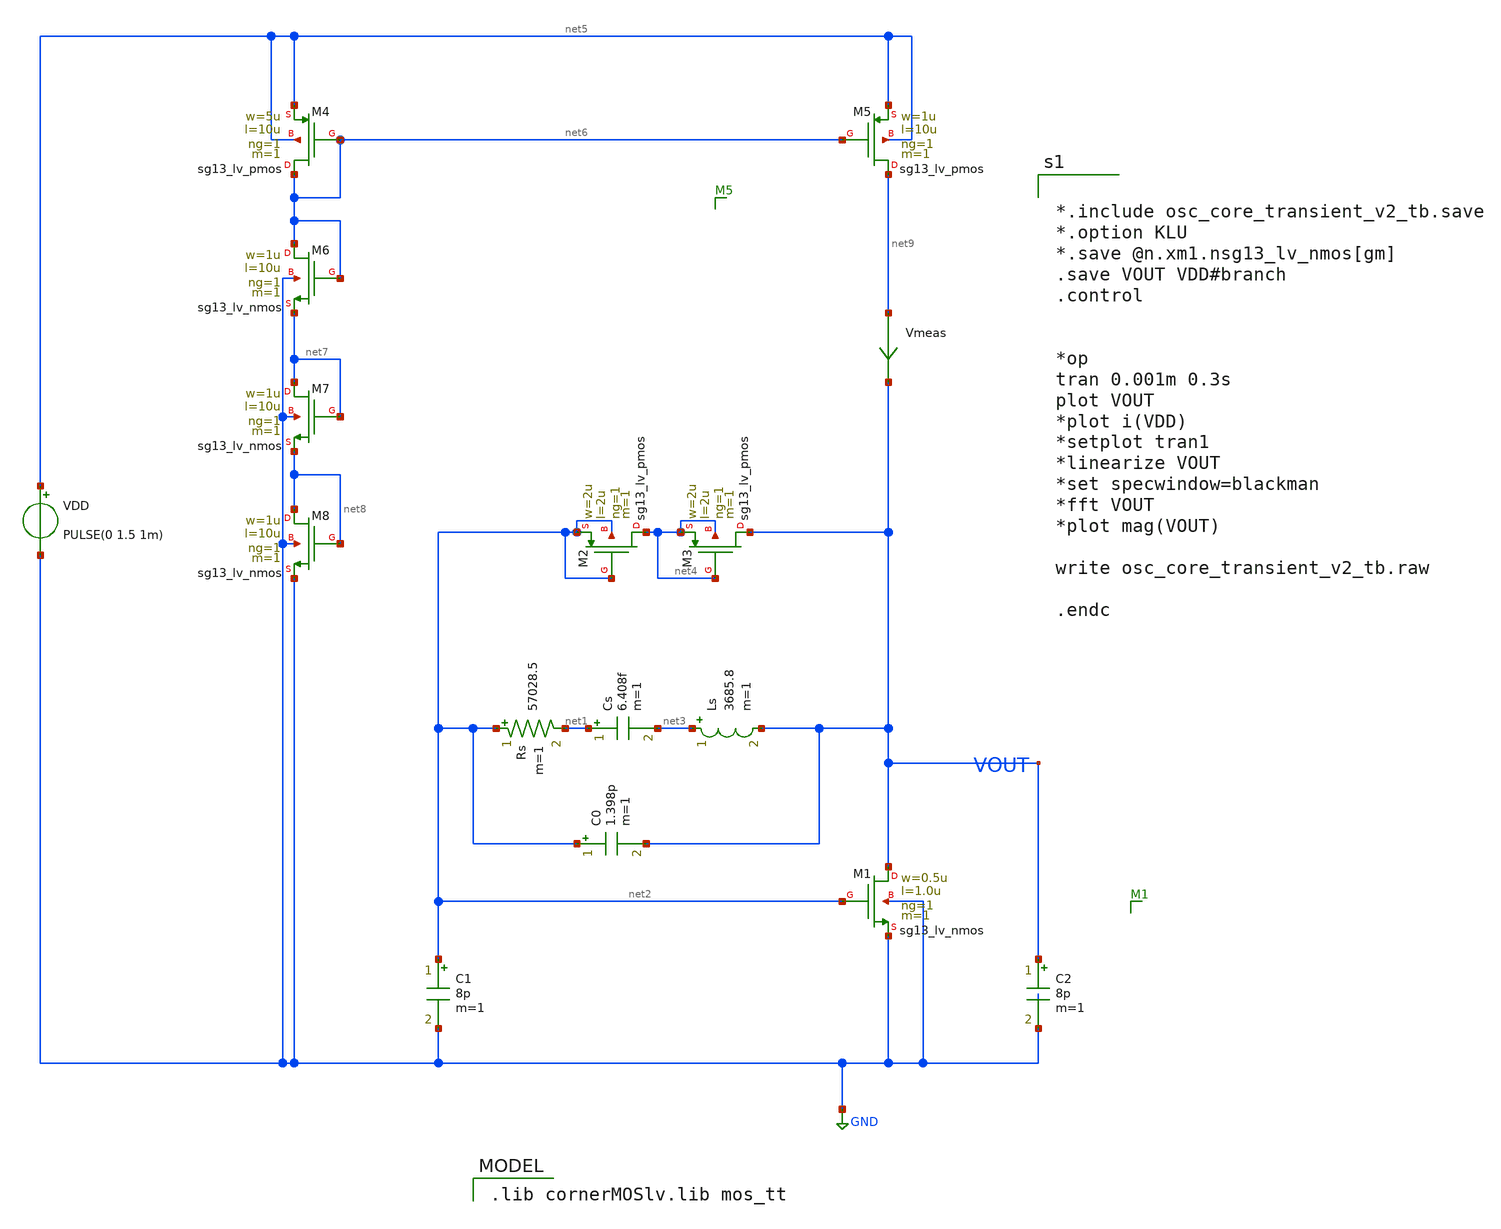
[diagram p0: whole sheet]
** sch_path: osc_core_transient_v2_tb.sch
**.subckt osc_core_transient_v2_tb
XM1 VOUT net2 GND GND sg13_lv_nmos w=0.5u l=1.0u ng=1 m=1 mm_ok=1
C1 net2 GND 8p m=1
C2 VOUT GND 8p m=1
Rs net2 net1 57028.5 m=1
Cs net1 net3 6.408f m=1
C0 net2 VOUT 1.398p m=1
Ls net3 VOUT 3685.8 m=1
VDD net5 GND PULSE(0 1.5 1m)
XM2 net4 net2 net2 net2 sg13_lv_pmos w=2u l=2u ng=1 m=1 mm_ok=1
XM3 VOUT net4 net4 net4 sg13_lv_pmos w=2u l=2u ng=1 m=1 mm_ok=1
XM4 net6 net6 net5 net5 sg13_lv_pmos w=5u l=10u ng=1 m=1 mm_ok=1
XM5 net9 net6 net5 net5 sg13_lv_pmos w=1u l=10u ng=1 m=1 mm_ok=1
XM6 net6 net6 net7 GND sg13_lv_nmos w=1u l=10u ng=1 m=1 mm_ok=1
XM7 net7 net7 net8 GND sg13_lv_nmos w=1u l=10u ng=1 m=1 mm_ok=1
XM8 net8 net8 GND GND sg13_lv_nmos w=1u l=10u ng=1 m=1 mm_ok=1
Vmeas net9 VOUT 0
.save i(vmeas)
**** begin user architecture code


*.include osc_core_transient_v2_tb.save
*.option KLU
*.save @n.xm1.nsg13_lv_nmos[gm]
.save VOUT VDD#branch
.control


*op
tran 0.001m 0.3s
plot VOUT
*plot i(VDD)
*setplot tran1
*linearize VOUT
*set specwindow=blackman
*fft VOUT
*plot mag(VOUT)

write osc_core_transient_v2_tb.raw

.endc


 .lib cornerMOSlv.lib mos_tt

**** end user architecture code
**.ends
.GLOBAL GND
.end
